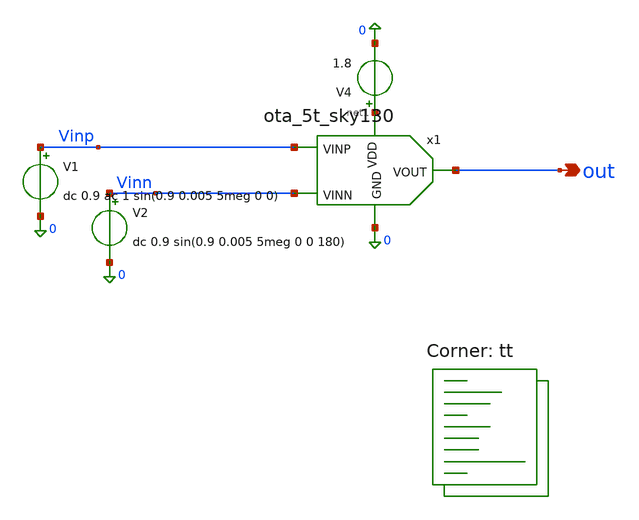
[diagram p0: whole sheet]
** sch_path: xschem/ota_5t_sky130_tb.sch
**.subckt ota_5t_sky130_tb out
*.opin out
V1 Vinp 0 dc 0.9 ac 1 sin(0.9 0.005 5meg 0 0)
V2 Vinn 0 dc 0.9 sin(0.9 0.005 5meg 0 0 180)
V4 net1 0 1.8
x1 net1 out Vinp Vinn 0 ota_5t_sky130
**** begin user architecture code
.lib $::SKYWATER_MODELS/sky130.lib.spice tt


.control
save all
tran 1n 400n
write ota5t_tran.raw
op
print @m.x1.xm2.msky130_fd_pr__nfet_01v8[gds] @m.x1.xm4.msky130_fd_pr__pfet_01v8[gds]
write ota5t_op.raw
ac dec 20 1k 100meg
write ota5t_ac.raw
.endc

**** end user architecture code
**.ends

* expanding   symbol:  ota_5t_sky130.sym # of pins=5
** sym_path: xschem/ota_5t_sky130.sym
** sch_path: xschem/ota_5t_sky130.sch
.subckt ota_5t_sky130 VDD VOUT VINP VINN GND
*.ipin VINP
*.ipin VINN
*.opin VOUT
*.ipin VDD
*.ipin GND
XM5 V5 VDD GND GND sky130_fd_pr__nfet_01v8 L=1.475 W=4 nf=1 ad='int((1 + 1)/2) * 4 / 1 * 0.29' as='int((1 + 2)/2) * 4 / 1 * 0.29'
+ pd='2*int((1 + 1)/2) * (4 / 1 + 0.29)' ps='2*int((1 + 2)/2) * (4 / 1 + 0.29)' nrd='0.29 / 4 ' nrs='0.29 / 4 '
+ sa=0 sb=0 sd=0 mult=1 m=1
XM1 net1 VINP V5 GND sky130_fd_pr__nfet_01v8 L=0.5 W=2 nf=1 ad='int((1 + 1)/2) * 2 / 1 * 0.29' as='int((1 + 2)/2) * 2 / 1 * 0.29'
+ pd='2*int((1 + 1)/2) * (2 / 1 + 0.29)' ps='2*int((1 + 2)/2) * (2 / 1 + 0.29)' nrd='0.29 / 2 ' nrs='0.29 / 2 '
+ sa=0 sb=0 sd=0 mult=1 m=1
XM2 VOUT VINN V5 GND sky130_fd_pr__nfet_01v8 L=0.5 W=2 nf=1 ad='int((1 + 1)/2) * 2 / 1 * 0.29' as='int((1 + 2)/2) * 2 / 1 * 0.29'
+ pd='2*int((1 + 1)/2) * (2 / 1 + 0.29)' ps='2*int((1 + 2)/2) * (2 / 1 + 0.29)' nrd='0.29 / 2 ' nrs='0.29 / 2 '
+ sa=0 sb=0 sd=0 mult=1 m=1
XM3 net1 net1 VDD VDD sky130_fd_pr__pfet_01v8 L=0.5 W=5 nf=1 ad='int((1 + 1)/2) * 5 / 1 * 0.29' as='int((1 + 2)/2) * 5 / 1 * 0.29'
+ pd='2*int((1 + 1)/2) * (5 / 1 + 0.29)' ps='2*int((1 + 2)/2) * (5 / 1 + 0.29)' nrd='0.29 / 5 ' nrs='0.29 / 5 '
+ sa=0 sb=0 sd=0 mult=1 m=1
XM4 VOUT net1 VDD VDD sky130_fd_pr__pfet_01v8 L=0.5 W=5 nf=1 ad='int((1 + 1)/2) * 5 / 1 * 0.29' as='int((1 + 2)/2) * 5 / 1 * 0.29'
+ pd='2*int((1 + 1)/2) * (5 / 1 + 0.29)' ps='2*int((1 + 2)/2) * (5 / 1 + 0.29)' nrd='0.29 / 5 ' nrs='0.29 / 5 '
+ sa=0 sb=0 sd=0 mult=1 m=1
XM6 VDD VDD GND GND sky130_fd_pr__nfet_01v8 L=0.5 W=4 nf=1 ad='int((1 + 1)/2) * 4 / 1 * 0.29' as='int((1 + 2)/2) * 4 / 1 * 0.29'
+ pd='2*int((1 + 1)/2) * (4 / 1 + 0.29)' ps='2*int((1 + 2)/2) * (4 / 1 + 0.29)' nrd='0.29 / 4 ' nrs='0.29 / 4 '
+ sa=0 sb=0 sd=0 mult=1 m=1
.ends

.end
